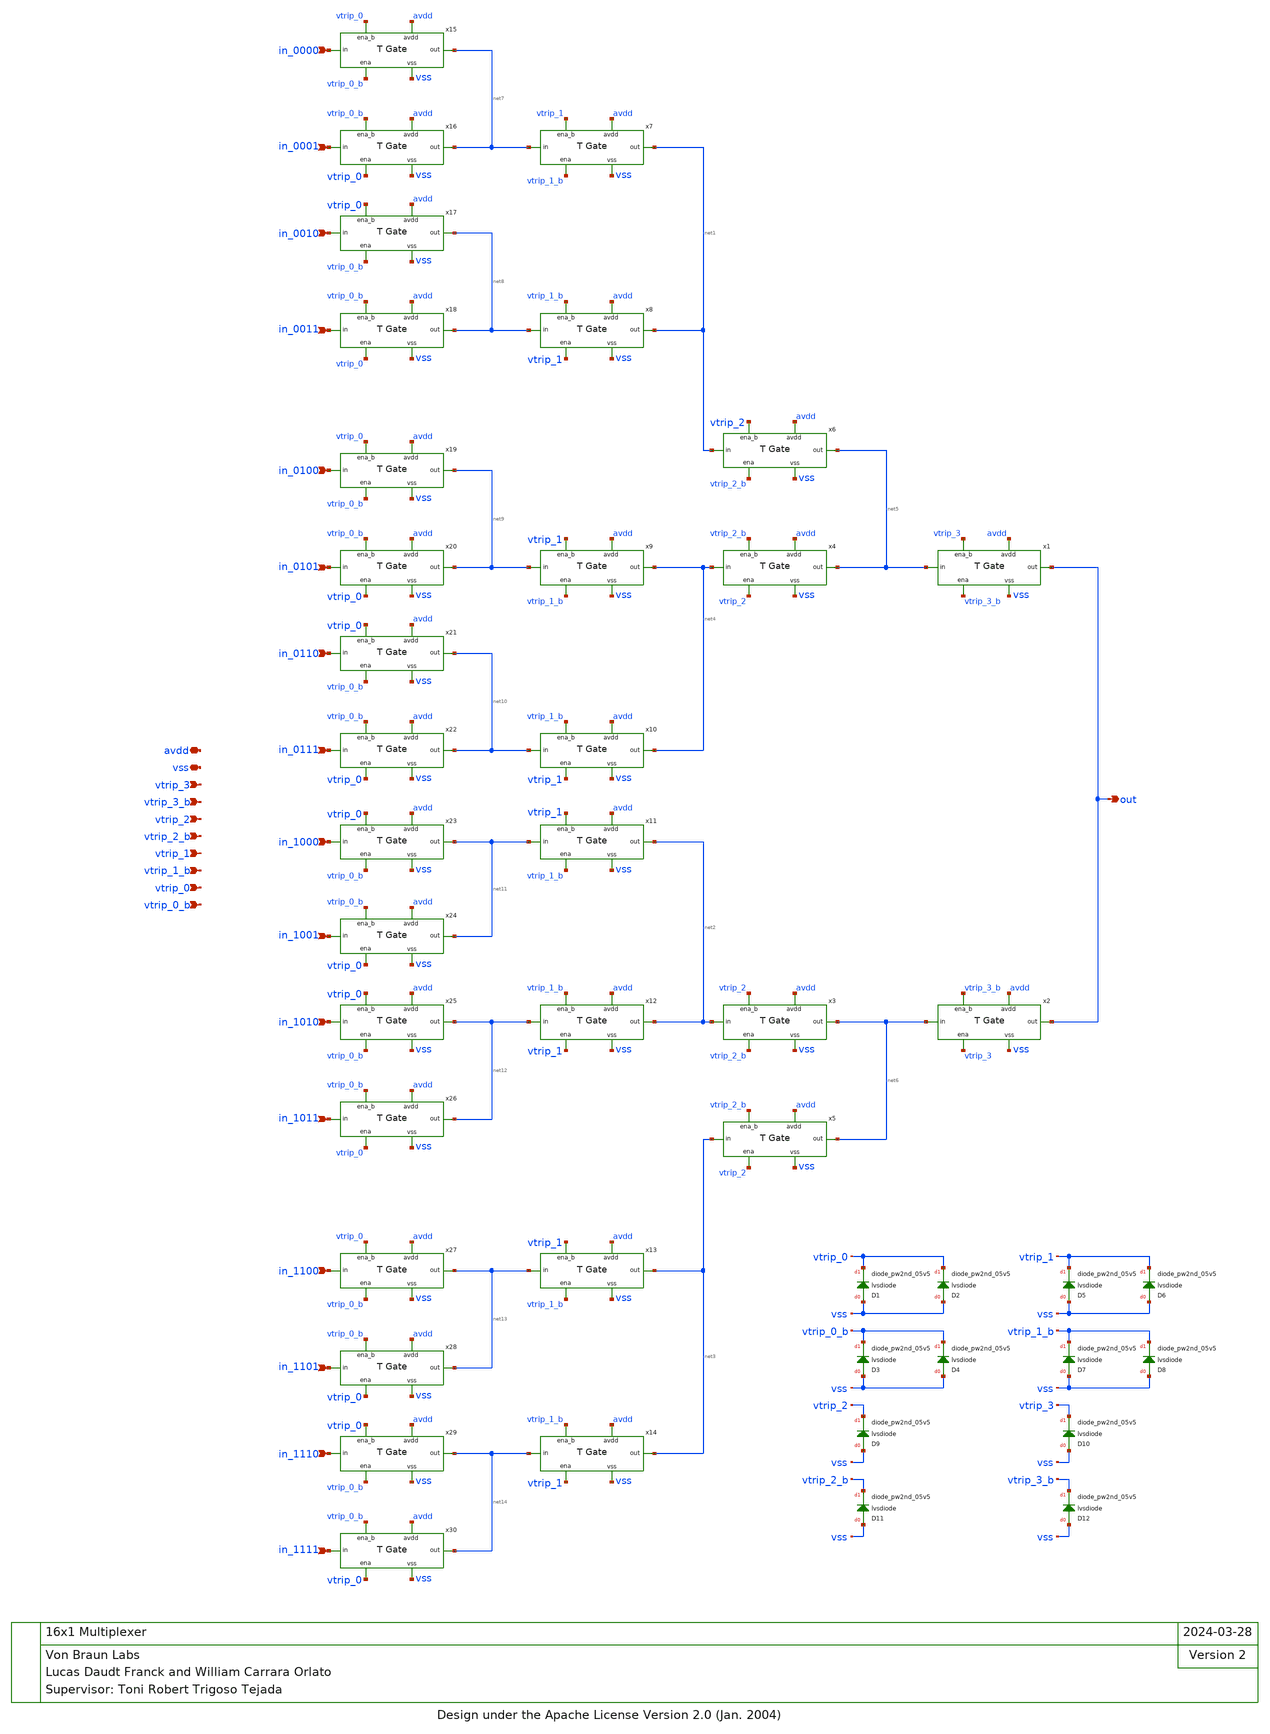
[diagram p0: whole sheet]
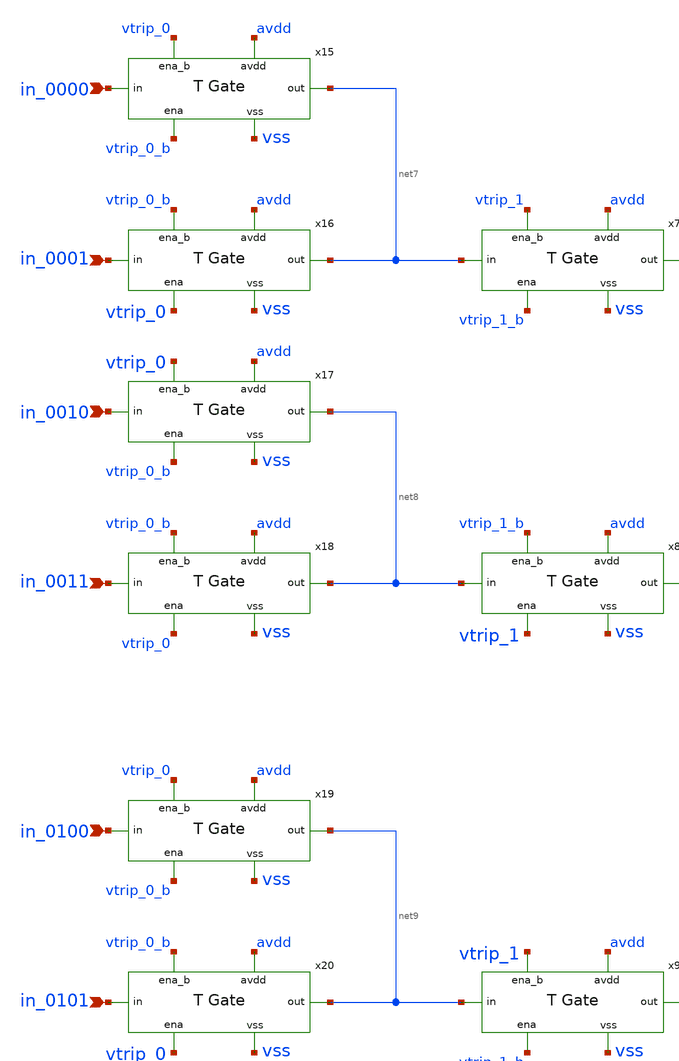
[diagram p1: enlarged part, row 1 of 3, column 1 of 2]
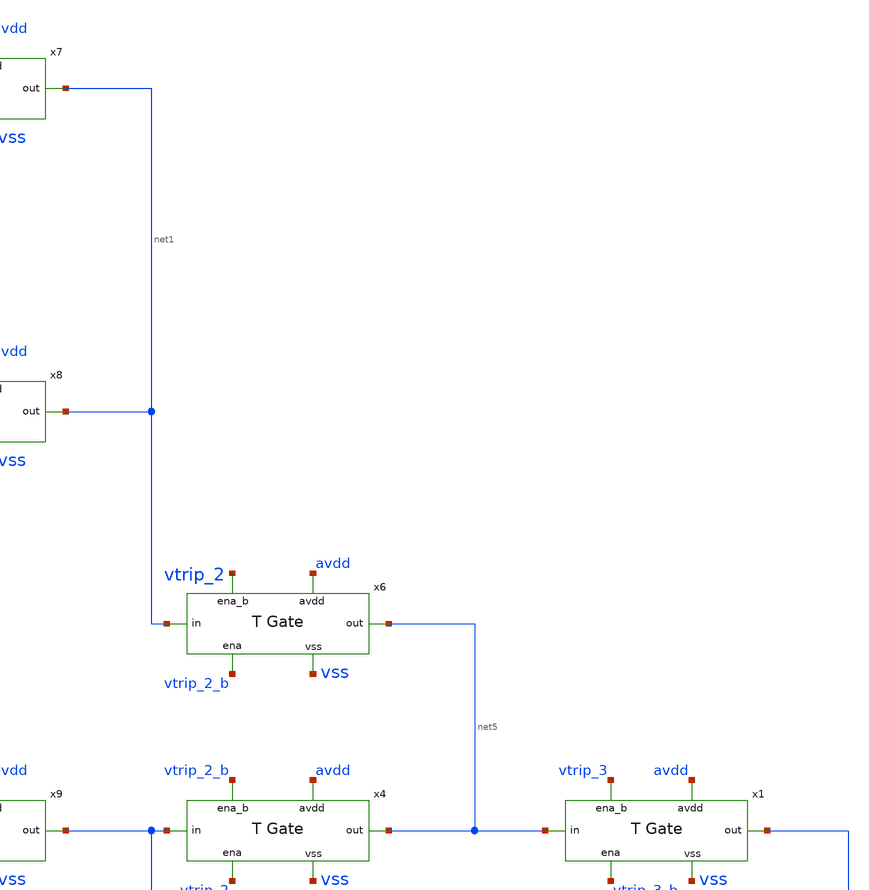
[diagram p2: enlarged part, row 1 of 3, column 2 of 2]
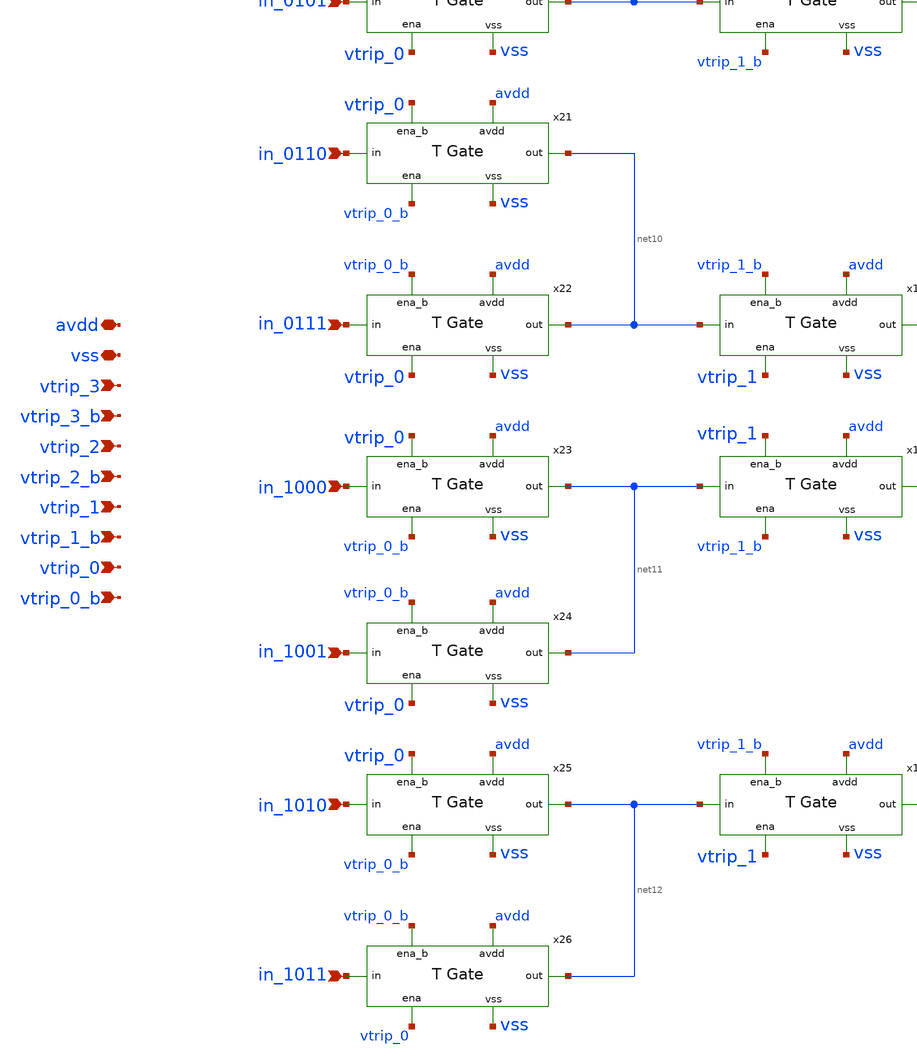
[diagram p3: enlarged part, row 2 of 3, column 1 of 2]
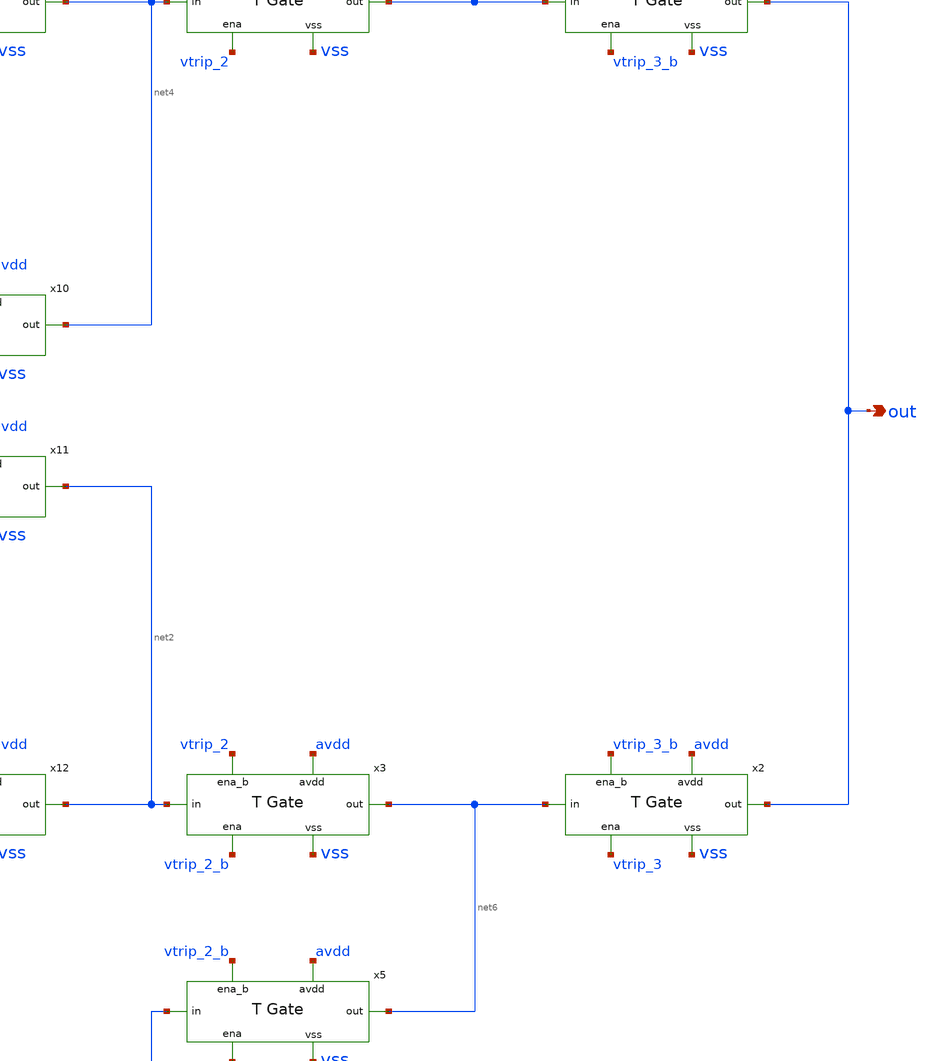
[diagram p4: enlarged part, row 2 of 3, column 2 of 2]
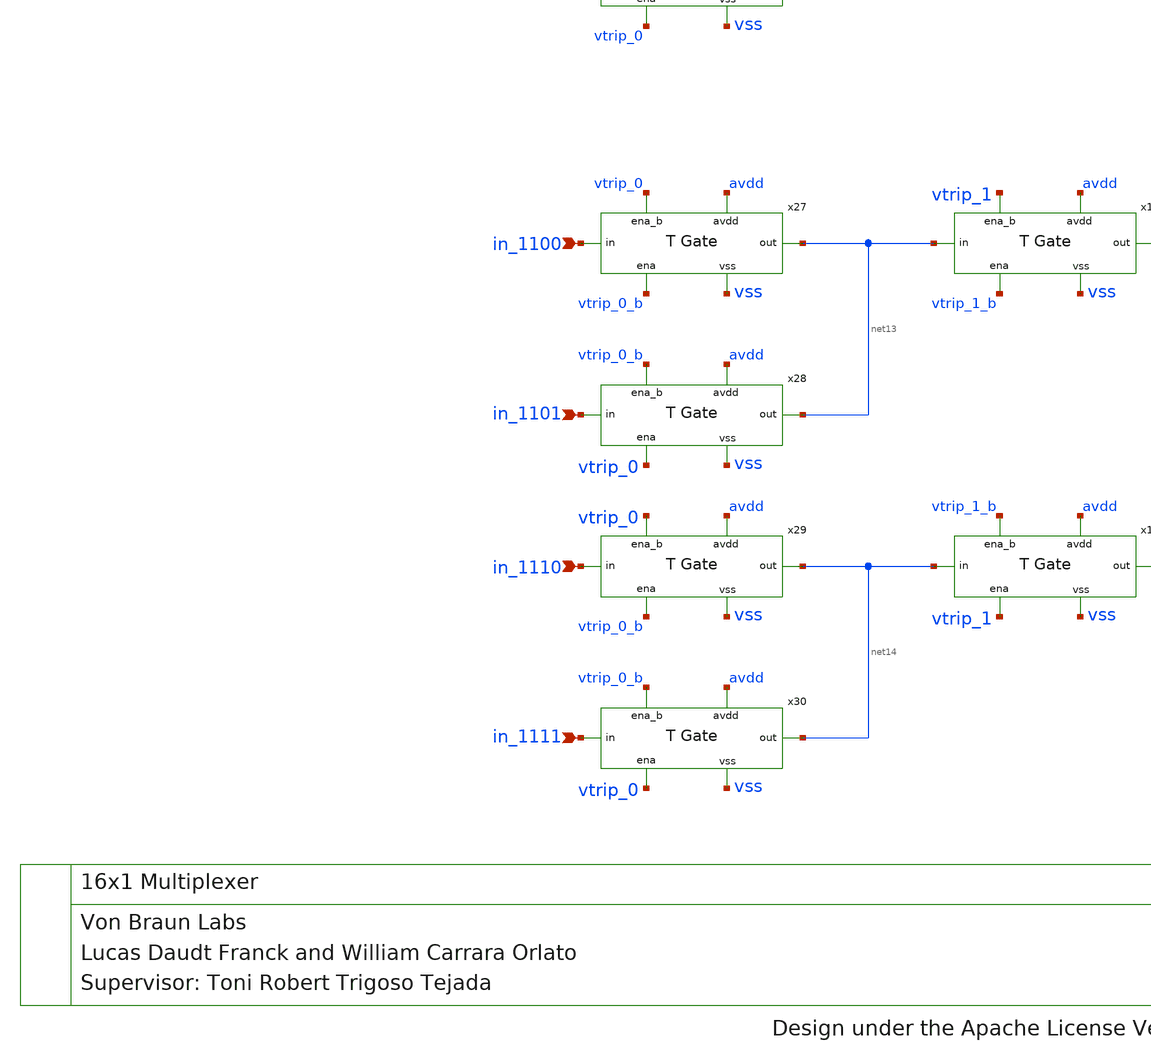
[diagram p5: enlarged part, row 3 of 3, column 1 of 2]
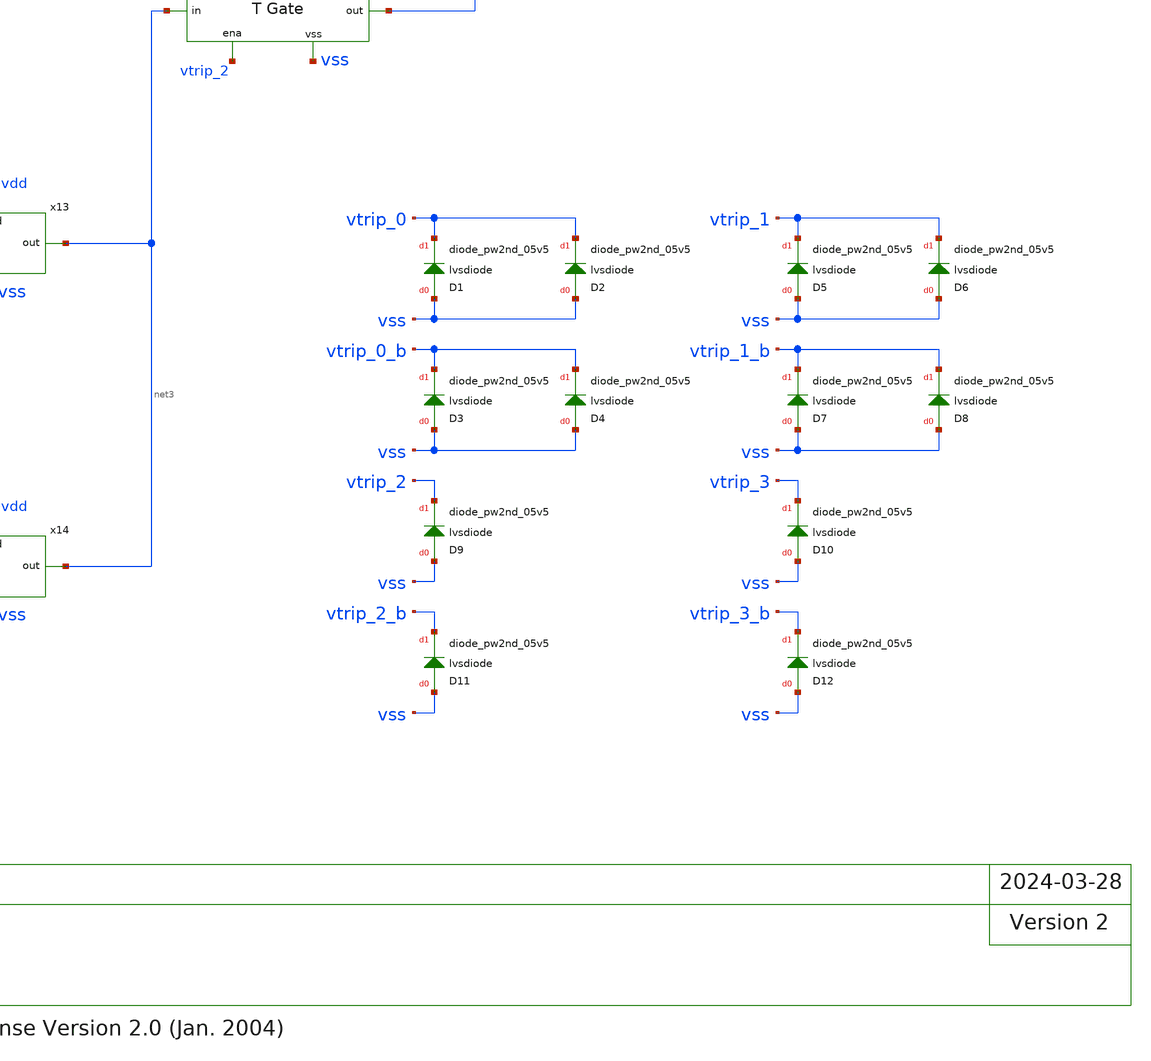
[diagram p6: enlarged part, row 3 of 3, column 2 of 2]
** sch_path: xschem/multiplexer.sch
* Design under the Apache License Version 2.0 (Jan. 2004)
**.subckt multiplexer in_0000 in_0001 in_0010 in_0011 in_0100 in_0101 in_0110 in_0111 in_1000
*+ in_1001 in_1010 in_1011 in_1110 in_1111 in_1100 in_1101 out vtrip_3 vtrip_3_b vtrip_2 vtrip_2_b vtrip_1
*+ vtrip_1_b vtrip_0 vtrip_0_b avdd vss
*.ipin in_0000
*.ipin in_0001
*.ipin in_0010
*.ipin in_0011
*.ipin in_0100
*.ipin in_0101
*.ipin in_0110
*.ipin in_0111
*.ipin in_1000
*.ipin in_1001
*.ipin in_1010
*.ipin in_1011
*.ipin in_1110
*.ipin in_1111
*.ipin in_1100
*.ipin in_1101
*.opin out
*.ipin vtrip_3
*.ipin vtrip_3_b
*.ipin vtrip_2
*.ipin vtrip_2_b
*.ipin vtrip_1
*.ipin vtrip_1_b
*.ipin vtrip_0
*.ipin vtrip_0_b
*.iopin avdd
*.iopin vss
x1 net5 vtrip_3 vtrip_3_b avdd vss out trans_gate_mux
x2 net6 vtrip_3_b vtrip_3 avdd vss out trans_gate_mux
x3 net2 vtrip_2 vtrip_2_b avdd vss net6 trans_gate_mux
x4 net4 vtrip_2_b vtrip_2 avdd vss net5 trans_gate_mux
x5 net3 vtrip_2_b vtrip_2 avdd vss net6 trans_gate_mux
x6 net1 vtrip_2 vtrip_2_b avdd vss net5 trans_gate_mux
x7 net7 vtrip_1 vtrip_1_b avdd vss net1 trans_gate_mux
x8 net8 vtrip_1_b vtrip_1 avdd vss net1 trans_gate_mux
x9 net9 vtrip_1 vtrip_1_b avdd vss net4 trans_gate_mux
x10 net10 vtrip_1_b vtrip_1 avdd vss net4 trans_gate_mux
x11 net11 vtrip_1 vtrip_1_b avdd vss net2 trans_gate_mux
x12 net12 vtrip_1_b vtrip_1 avdd vss net2 trans_gate_mux
x13 net13 vtrip_1 vtrip_1_b avdd vss net3 trans_gate_mux
x14 net14 vtrip_1_b vtrip_1 avdd vss net3 trans_gate_mux
x15 in_0000 vtrip_0 vtrip_0_b avdd vss net7 trans_gate_mux
x16 in_0001 vtrip_0_b vtrip_0 avdd vss net7 trans_gate_mux
x17 in_0010 vtrip_0 vtrip_0_b avdd vss net8 trans_gate_mux
x18 in_0011 vtrip_0_b vtrip_0 avdd vss net8 trans_gate_mux
x19 in_0100 vtrip_0 vtrip_0_b avdd vss net9 trans_gate_mux
x20 in_0101 vtrip_0_b vtrip_0 avdd vss net9 trans_gate_mux
x21 in_0110 vtrip_0 vtrip_0_b avdd vss net10 trans_gate_mux
x22 in_0111 vtrip_0_b vtrip_0 avdd vss net10 trans_gate_mux
x23 in_1000 vtrip_0 vtrip_0_b avdd vss net11 trans_gate_mux
x24 in_1001 vtrip_0_b vtrip_0 avdd vss net11 trans_gate_mux
x25 in_1010 vtrip_0 vtrip_0_b avdd vss net12 trans_gate_mux
x26 in_1011 vtrip_0_b vtrip_0 avdd vss net12 trans_gate_mux
x27 in_1100 vtrip_0 vtrip_0_b avdd vss net13 trans_gate_mux
x28 in_1101 vtrip_0_b vtrip_0 avdd vss net13 trans_gate_mux
x29 in_1110 vtrip_0 vtrip_0_b avdd vss net14 trans_gate_mux
x30 in_1111 vtrip_0_b vtrip_0 avdd vss net14 trans_gate_mux
D1 vss vtrip_0 sky130_fd_pr__diode_pw2nd_05v5 area=3.15e11
D2 vss vtrip_0 sky130_fd_pr__diode_pw2nd_05v5 area=3.15e11
D3 vss vtrip_0_b sky130_fd_pr__diode_pw2nd_05v5 area=3.15e11
D4 vss vtrip_0_b sky130_fd_pr__diode_pw2nd_05v5 area=3.15e11
D5 vss vtrip_1 sky130_fd_pr__diode_pw2nd_05v5 area=3.15e11
D6 vss vtrip_1 sky130_fd_pr__diode_pw2nd_05v5 area=3.15e11
D7 vss vtrip_1_b sky130_fd_pr__diode_pw2nd_05v5 area=3.15e11
D8 vss vtrip_1_b sky130_fd_pr__diode_pw2nd_05v5 area=3.15e11
D9 vss vtrip_2 sky130_fd_pr__diode_pw2nd_05v5 area=3.15e11
D11 vss vtrip_2_b sky130_fd_pr__diode_pw2nd_05v5 area=3.15e11
D10 vss vtrip_3 sky130_fd_pr__diode_pw2nd_05v5 area=3.15e11
D12 vss vtrip_3_b sky130_fd_pr__diode_pw2nd_05v5 area=3.15e11
**.ends

* expanding   symbol:  trans_gate_mux.sym # of pins=6
** sym_path: xschem/trans_gate_mux.sym
** sch_path: xschem/trans_gate_mux.sch
.subckt trans_gate_mux in ena_b ena avdd vss out
*.iopin avdd
*.iopin vss
*.ipin ena
*.ipin ena_b
*.ipin in
*.opin out
XM1 in ena out vss sky130_fd_pr__nfet_g5v0d10v5 L=3 W=1 nf=1 ad='int((nf+1)/2) * W/nf * 0.29' as='int((nf+2)/2) * W/nf * 0.29'
+ pd='2*int((nf+1)/2) * (W/nf + 0.29)' ps='2*int((nf+2)/2) * (W/nf + 0.29)' nrd='0.29 / W' nrs='0.29 / W'
+ sa=0 sb=0 sd=0 mult=1 m=1
XM2 in ena_b out avdd sky130_fd_pr__pfet_g5v0d10v5 L=3 W=1 nf=1 ad='int((nf+1)/2) * W/nf * 0.29' as='int((nf+2)/2) * W/nf * 0.29'
+ pd='2*int((nf+1)/2) * (W/nf + 0.29)' ps='2*int((nf+2)/2) * (W/nf + 0.29)' nrd='0.29 / W' nrs='0.29 / W'
+ sa=0 sb=0 sd=0 mult=1 m=1
.ends

.end
